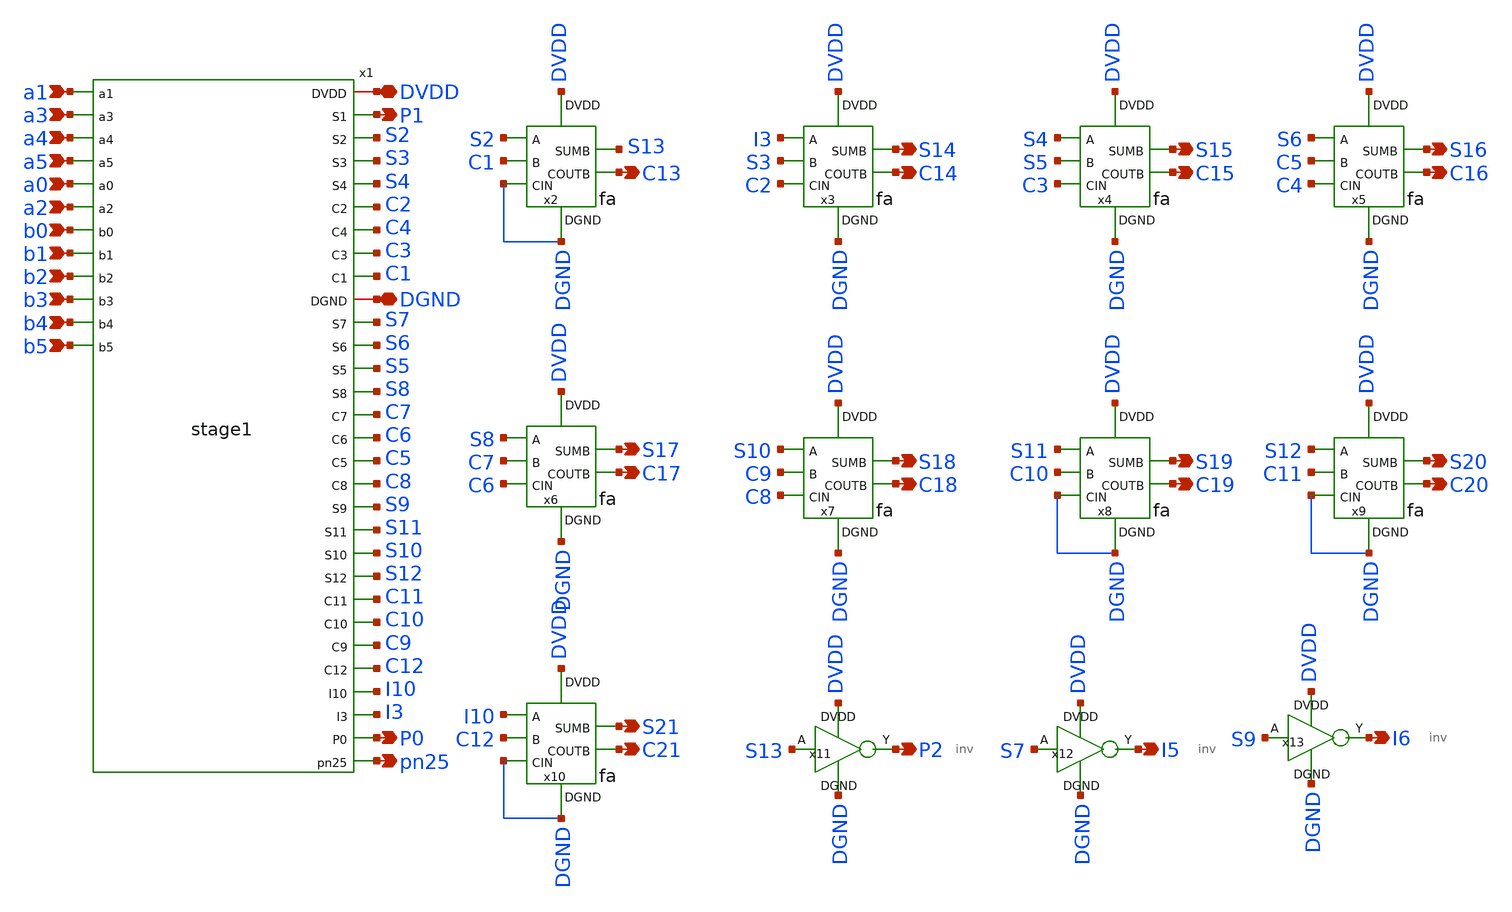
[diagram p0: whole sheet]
** sch_path: xschem/stage2.sch
**.subckt stage2 a1 a3 a4 a5 a0 a2 b0 b1 b2 b3 b4 b5 P0 DGND DVDD P1 C13 S14 C14 S15 C15 S16 C16 S17
*+ C17 S18 C18 S19 C19 S20 C20 S21 C21 P2 I5 I6 pn25
*.ipin a1
*.ipin a3
*.ipin a4
*.ipin a5
*.ipin a0
*.ipin a2
*.ipin b0
*.ipin b1
*.ipin b2
*.ipin b3
*.ipin b4
*.ipin b5
*.opin P0
*.iopin DGND
*.iopin DVDD
*.opin P1
*.opin C13
*.opin S14
*.opin C14
*.opin S15
*.opin C15
*.opin S16
*.opin C16
*.opin S17
*.opin C17
*.opin S18
*.opin C18
*.opin S19
*.opin C19
*.opin S20
*.opin C20
*.opin S21
*.opin C21
*.opin P2
*.opin I5
*.opin I6
*.opin pn25
x2 DVDD DGND S2 C1 DGND C13 S13 fa
x3 DVDD DGND I3 S3 C2 C14 S14 fa
x4 DVDD DGND S4 S5 C3 C15 S15 fa
x5 DVDD DGND S6 C5 C4 C16 S16 fa
x6 DVDD DGND S8 C7 C6 C17 S17 fa
x7 DVDD DGND S10 C9 C8 C18 S18 fa
x8 DVDD DGND S11 C10 DGND C19 S19 fa
x9 DVDD DGND S12 C11 DGND C20 S20 fa
x10 DVDD DGND I10 C12 DGND C21 S21 fa
x11 S13 P2 DVDD DGND inv
x12 S7 I5 DVDD DGND inv
x13 S9 I6 DVDD DGND inv
x1 DVDD a1 P1 S2 S3 a3 a4 a5 a0 S4 a2 C2 C4 b0 C3 C1 DGND S7 S6 S5 S8 b1 C7 C6 C5 C8 b2 S9 S11 S10
+ S12 C11 C10 C9 C12 b3 I10 I3 P0 b4 pn25 b5 stage1
**.ends
.end
